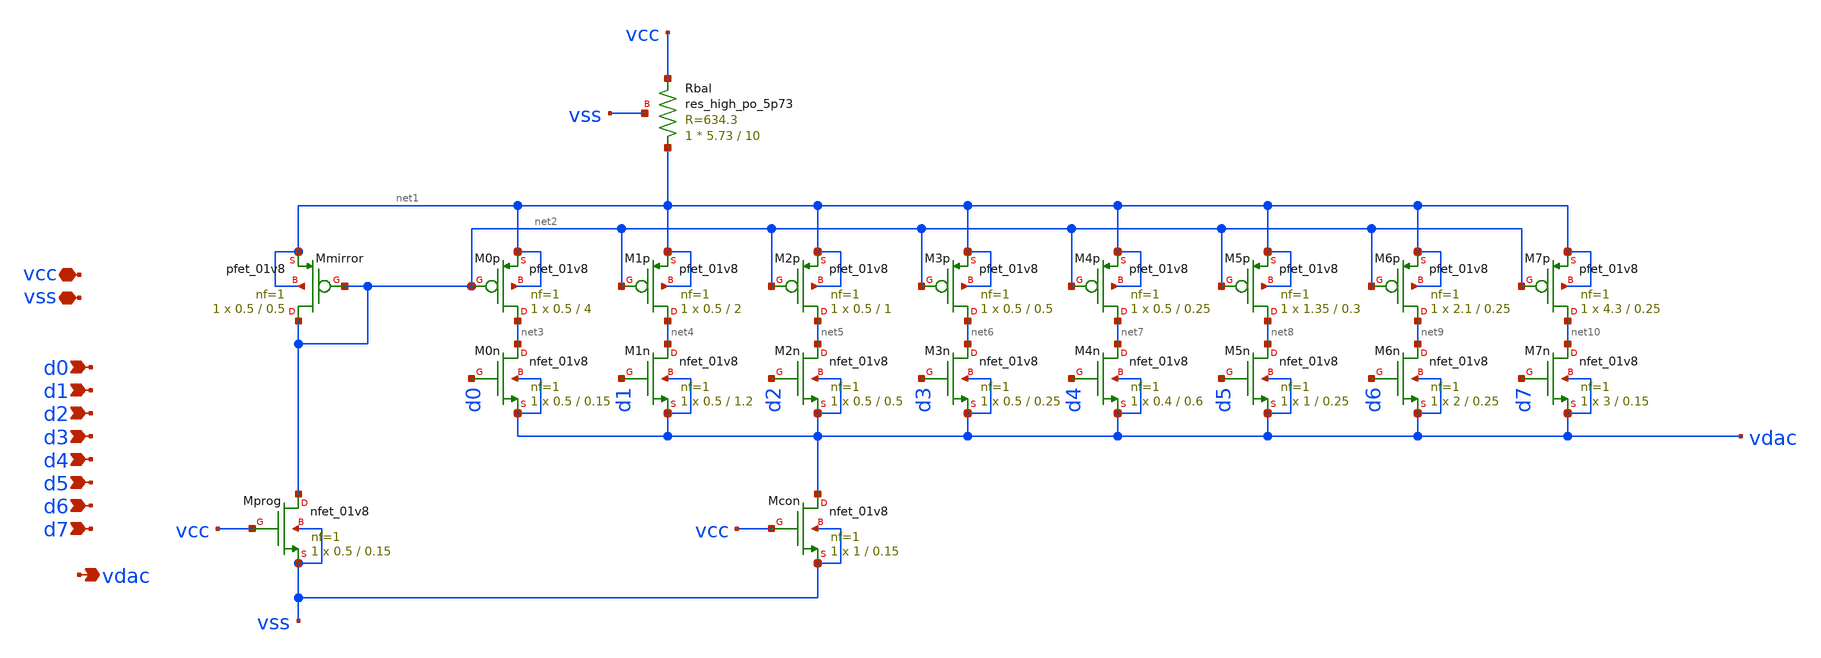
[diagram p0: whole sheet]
** sch_path: xschem/bdac.sch
**.subckt bdac d0 vdac vcc d1 d2 d3 d4 d5 d6 d7 vss
*.ipin d0
*.opin vdac
*.iopin vcc
*.ipin d1
*.ipin d2
*.ipin d3
*.ipin d4
*.ipin d5
*.ipin d6
*.ipin d7
*.iopin vss
XM2p net5 net2 net1 net1 sky130_fd_pr__pfet_01v8 L=1 W=0.5 nf=1 ad='int((nf+1)/2) * W/nf * 0.29' as='int((nf+2)/2) * W/nf * 0.29'
+ pd='2*int((nf+1)/2) * (W/nf + 0.29)' ps='2*int((nf+2)/2) * (W/nf + 0.29)' nrd='0.29 / W' nrs='0.29 / W'
+ sa=0 sb=0 sd=0 mult=1 m=1
XM1p net4 net2 net1 net1 sky130_fd_pr__pfet_01v8 L=2 W=0.5 nf=1 ad='int((nf+1)/2) * W/nf * 0.29' as='int((nf+2)/2) * W/nf * 0.29'
+ pd='2*int((nf+1)/2) * (W/nf + 0.29)' ps='2*int((nf+2)/2) * (W/nf + 0.29)' nrd='0.29 / W' nrs='0.29 / W'
+ sa=0 sb=0 sd=0 mult=1 m=1
XM0p net3 net2 net1 net1 sky130_fd_pr__pfet_01v8 L=4 W=0.5 nf=1 ad='int((nf+1)/2) * W/nf * 0.29' as='int((nf+2)/2) * W/nf * 0.29'
+ pd='2*int((nf+1)/2) * (W/nf + 0.29)' ps='2*int((nf+2)/2) * (W/nf + 0.29)' nrd='0.29 / W' nrs='0.29 / W'
+ sa=0 sb=0 sd=0 mult=1 m=1
XMmirror net2 net2 net1 net1 sky130_fd_pr__pfet_01v8 L=0.5 W=0.5 nf=1 ad='int((nf+1)/2) * W/nf * 0.29'
+ as='int((nf+2)/2) * W/nf * 0.29' pd='2*int((nf+1)/2) * (W/nf + 0.29)' ps='2*int((nf+2)/2) * (W/nf + 0.29)'
+ nrd='0.29 / W' nrs='0.29 / W' sa=0 sb=0 sd=0 mult=1 m=1
XM0n net3 d0 vdac vdac sky130_fd_pr__nfet_01v8 L=0.15 W=0.5 nf=1 ad='int((nf+1)/2) * W/nf * 0.29' as='int((nf+2)/2) * W/nf * 0.29'
+ pd='2*int((nf+1)/2) * (W/nf + 0.29)' ps='2*int((nf+2)/2) * (W/nf + 0.29)' nrd='0.29 / W' nrs='0.29 / W'
+ sa=0 sb=0 sd=0 mult=1 m=1
XM1n net4 d1 vdac vdac sky130_fd_pr__nfet_01v8 L=1.2 W=0.5 nf=1 ad='int((nf+1)/2) * W/nf * 0.29' as='int((nf+2)/2) * W/nf * 0.29'
+ pd='2*int((nf+1)/2) * (W/nf + 0.29)' ps='2*int((nf+2)/2) * (W/nf + 0.29)' nrd='0.29 / W' nrs='0.29 / W'
+ sa=0 sb=0 sd=0 mult=1 m=1
XM2n net5 d2 vdac vdac sky130_fd_pr__nfet_01v8 L=0.5 W=0.5 nf=1 ad='int((nf+1)/2) * W/nf * 0.29' as='int((nf+2)/2) * W/nf * 0.29'
+ pd='2*int((nf+1)/2) * (W/nf + 0.29)' ps='2*int((nf+2)/2) * (W/nf + 0.29)' nrd='0.29 / W' nrs='0.29 / W'
+ sa=0 sb=0 sd=0 mult=1 m=1
XMcon vdac vcc vss vss sky130_fd_pr__nfet_01v8 L=0.15 W=1 nf=1 ad='int((nf+1)/2) * W/nf * 0.29' as='int((nf+2)/2) * W/nf * 0.29'
+ pd='2*int((nf+1)/2) * (W/nf + 0.29)' ps='2*int((nf+2)/2) * (W/nf + 0.29)' nrd='0.29 / W' nrs='0.29 / W'
+ sa=0 sb=0 sd=0 mult=1 m=1
XM3p net6 net2 net1 net1 sky130_fd_pr__pfet_01v8 L=0.5 W=0.5 nf=1 ad='int((nf+1)/2) * W/nf * 0.29' as='int((nf+2)/2) * W/nf * 0.29'
+ pd='2*int((nf+1)/2) * (W/nf + 0.29)' ps='2*int((nf+2)/2) * (W/nf + 0.29)' nrd='0.29 / W' nrs='0.29 / W'
+ sa=0 sb=0 sd=0 mult=1 m=1
XM3n net6 d3 vdac vdac sky130_fd_pr__nfet_01v8 L=0.25 W=0.5 nf=1 ad='int((nf+1)/2) * W/nf * 0.29' as='int((nf+2)/2) * W/nf * 0.29'
+ pd='2*int((nf+1)/2) * (W/nf + 0.29)' ps='2*int((nf+2)/2) * (W/nf + 0.29)' nrd='0.29 / W' nrs='0.29 / W'
+ sa=0 sb=0 sd=0 mult=1 m=1
XM4p net7 net2 net1 net1 sky130_fd_pr__pfet_01v8 L=0.25 W=0.5 nf=1 ad='int((nf+1)/2) * W/nf * 0.29' as='int((nf+2)/2) * W/nf * 0.29'
+ pd='2*int((nf+1)/2) * (W/nf + 0.29)' ps='2*int((nf+2)/2) * (W/nf + 0.29)' nrd='0.29 / W' nrs='0.29 / W'
+ sa=0 sb=0 sd=0 mult=1 m=1
XM4n net7 d4 vdac vdac sky130_fd_pr__nfet_01v8 L=0.6 W=0.4 nf=1 ad='int((nf+1)/2) * W/nf * 0.29' as='int((nf+2)/2) * W/nf * 0.29'
+ pd='2*int((nf+1)/2) * (W/nf + 0.29)' ps='2*int((nf+2)/2) * (W/nf + 0.29)' nrd='0.29 / W' nrs='0.29 / W'
+ sa=0 sb=0 sd=0 mult=1 m=1
XM5p net8 net2 net1 net1 sky130_fd_pr__pfet_01v8 L=0.3 W=1.35 nf=1 ad='int((nf+1)/2) * W/nf * 0.29' as='int((nf+2)/2) * W/nf * 0.29'
+ pd='2*int((nf+1)/2) * (W/nf + 0.29)' ps='2*int((nf+2)/2) * (W/nf + 0.29)' nrd='0.29 / W' nrs='0.29 / W'
+ sa=0 sb=0 sd=0 mult=1 m=1
XM5n net8 d5 vdac vdac sky130_fd_pr__nfet_01v8 L=0.25 W=1 nf=1 ad='int((nf+1)/2) * W/nf * 0.29' as='int((nf+2)/2) * W/nf * 0.29'
+ pd='2*int((nf+1)/2) * (W/nf + 0.29)' ps='2*int((nf+2)/2) * (W/nf + 0.29)' nrd='0.29 / W' nrs='0.29 / W'
+ sa=0 sb=0 sd=0 mult=1 m=1
XM6p net9 net2 net1 net1 sky130_fd_pr__pfet_01v8 L=0.25 W=2.1 nf=1 ad='int((nf+1)/2) * W/nf * 0.29' as='int((nf+2)/2) * W/nf * 0.29'
+ pd='2*int((nf+1)/2) * (W/nf + 0.29)' ps='2*int((nf+2)/2) * (W/nf + 0.29)' nrd='0.29 / W' nrs='0.29 / W'
+ sa=0 sb=0 sd=0 mult=1 m=1
XM6n net9 d6 vdac vdac sky130_fd_pr__nfet_01v8 L=0.25 W=2 nf=1 ad='int((nf+1)/2) * W/nf * 0.29' as='int((nf+2)/2) * W/nf * 0.29'
+ pd='2*int((nf+1)/2) * (W/nf + 0.29)' ps='2*int((nf+2)/2) * (W/nf + 0.29)' nrd='0.29 / W' nrs='0.29 / W'
+ sa=0 sb=0 sd=0 mult=1 m=1
XM7p net10 net2 net1 net1 sky130_fd_pr__pfet_01v8 L=0.25 W=4.3 nf=1 ad='int((nf+1)/2) * W/nf * 0.29'
+ as='int((nf+2)/2) * W/nf * 0.29' pd='2*int((nf+1)/2) * (W/nf + 0.29)' ps='2*int((nf+2)/2) * (W/nf + 0.29)'
+ nrd='0.29 / W' nrs='0.29 / W' sa=0 sb=0 sd=0 mult=1 m=1
XM7n net10 d7 vdac vdac sky130_fd_pr__nfet_01v8 L=0.15 W=3 nf=1 ad='int((nf+1)/2) * W/nf * 0.29' as='int((nf+2)/2) * W/nf * 0.29'
+ pd='2*int((nf+1)/2) * (W/nf + 0.29)' ps='2*int((nf+2)/2) * (W/nf + 0.29)' nrd='0.29 / W' nrs='0.29 / W'
+ sa=0 sb=0 sd=0 mult=1 m=1
XMprog net2 vcc vss vss sky130_fd_pr__nfet_01v8 L=0.15 W=0.5 nf=1 ad='int((nf+1)/2) * W/nf * 0.29' as='int((nf+2)/2) * W/nf * 0.29'
+ pd='2*int((nf+1)/2) * (W/nf + 0.29)' ps='2*int((nf+2)/2) * (W/nf + 0.29)' nrd='0.29 / W' nrs='0.29 / W'
+ sa=0 sb=0 sd=0 mult=1 m=1
XRbal net1 vcc vss sky130_fd_pr__res_high_po_5p73 L=10 mult=1 m=1
**.ends
.end
